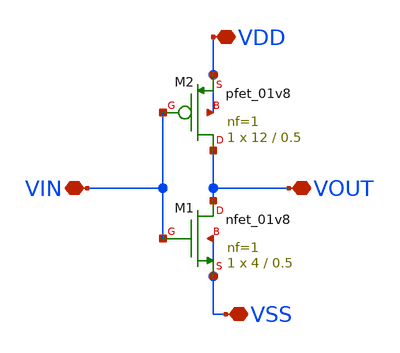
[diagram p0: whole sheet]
** sch_path: xschem/DC_DC_Converter_xschem/OTHERS/DC_DC_Converter_6/revised_delay-block/inverter_delay.sch
**.subckt inverter_delay VDD VOUT VSS VIN
*.iopin VDD
*.iopin VOUT
*.iopin VSS
*.iopin VIN
XM1 VOUT VIN VSS VSS sky130_fd_pr__nfet_01v8 L=0.5 W=4 nf=1 ad='int((nf+1)/2) * W/nf * 0.29' as='int((nf+2)/2) * W/nf * 0.29'
+ pd='2*int((nf+1)/2) * (W/nf + 0.29)' ps='2*int((nf+2)/2) * (W/nf + 0.29)' nrd='0.29 / W' nrs='0.29 / W'
+ sa=0 sb=0 sd=0 mult=1 m=1
XM2 VOUT VIN VDD VDD sky130_fd_pr__pfet_01v8 L=0.5 W=12 nf=1 ad='int((nf+1)/2) * W/nf * 0.29' as='int((nf+2)/2) * W/nf * 0.29'
+ pd='2*int((nf+1)/2) * (W/nf + 0.29)' ps='2*int((nf+2)/2) * (W/nf + 0.29)' nrd='0.29 / W' nrs='0.29 / W'
+ sa=0 sb=0 sd=0 mult=1 m=1
**.ends
.end
